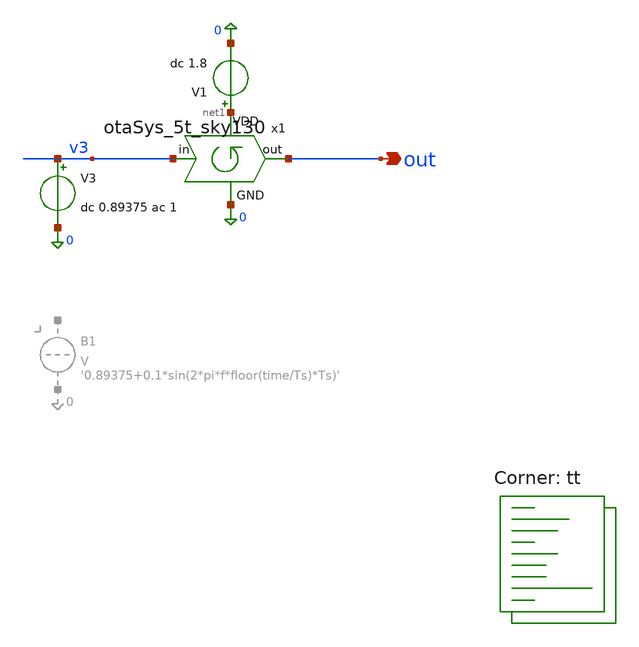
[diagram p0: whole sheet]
** sch_path: xschem/otaSys_5t_sky130_tb.sch
**.subckt otaSys_5t_sky130_tb out
*.opin out
V3 v3 0 dc 0.89375 ac 1
x1 net1 v3 out 0 otaSys_5t_sky130
V1 net1 0 dc 1.8
**** begin user architecture code
.lib $::SKYWATER_MODELS/sky130.lib.spice tt


.control
save all
.param f=5Meg
.param Fs=20Meg
.param Ts={1/Fs}
tran 1n 60000n
write otaSys_5t_sky130_tb_tran.raw
op
print @m.x1.x4.xm2.msky130_fd_pr__nfet_01v8[id] @m.x1.x4.xm4.msky130_fd_pr__pfet_01v8[id]
write otaSys_5t_sky130_tb_op.raw
ac dec 20 1 100meg
write otaSys_5t_sky130_tb_ac.raw
.endc

**** end user architecture code
**.ends

* expanding   symbol:  otaSys_5t_sky130.sym # of pins=4
** sym_path: xschem/otaSys_5t_sky130.sym
** sch_path: xschem/otaSys_5t_sky130.sch
.subckt otaSys_5t_sky130 VDD in out GND
*.opin out
*.ipin in
*.ipin GND
*.ipin VDD
x1 VDD net1 net2 in GND ota_5t_sky130
x2 VDD out net1 net2 GND ota_5t_sky130
x3 VDD net1 net2 out GND ota_5t_sky130
x4 VDD out out net2 GND otaq_5t_sky130
XC1 net1 GND sky130_fd_pr__cap_mim_m3_1 W=30 L=30 MF=4 m=4
XR1 VDD net2 GND sky130_fd_pr__res_high_po_1p41 L=88.83 mult=1 m=1
XR2 net2 GND GND sky130_fd_pr__res_high_po_1p41 L=88.83 mult=1 m=1
XC2 out GND sky130_fd_pr__cap_mim_m3_1 W=24 L=24 MF=1 m=1
XC3 out GND sky130_fd_pr__cap_mim_m3_1 W=24 L=24 MF=1 m=1
.ends


* expanding   symbol:  ota_5t_sky130.sym # of pins=5
** sym_path: xschem/ota_5t_sky130.sym
** sch_path: xschem/ota_5t_sky130.sch
.subckt ota_5t_sky130 VDD VOUT VINP VINN GND
*.ipin VINP
*.ipin VINN
*.opin VOUT
*.ipin VDD
*.ipin GND
XM5 V5 VDD GND GND sky130_fd_pr__nfet_01v8 L=1.475 W=4 nf=1 ad='int((1 + 1)/2) * 4 / 1 * 0.29' as='int((1 + 2)/2) * 4 / 1 * 0.29'
+ pd='2*int((1 + 1)/2) * (4 / 1 + 0.29)' ps='2*int((1 + 2)/2) * (4 / 1 + 0.29)' nrd='0.29 / 4 ' nrs='0.29 / 4 '
+ sa=0 sb=0 sd=0 mult=1 m=1
XM1 net1 VINP V5 GND sky130_fd_pr__nfet_01v8 L=0.5 W=2 nf=1 ad='int((1 + 1)/2) * 2 / 1 * 0.29' as='int((1 + 2)/2) * 2 / 1 * 0.29'
+ pd='2*int((1 + 1)/2) * (2 / 1 + 0.29)' ps='2*int((1 + 2)/2) * (2 / 1 + 0.29)' nrd='0.29 / 2 ' nrs='0.29 / 2 '
+ sa=0 sb=0 sd=0 mult=1 m=1
XM2 VOUT VINN V5 GND sky130_fd_pr__nfet_01v8 L=0.5 W=2 nf=1 ad='int((1 + 1)/2) * 2 / 1 * 0.29' as='int((1 + 2)/2) * 2 / 1 * 0.29'
+ pd='2*int((1 + 1)/2) * (2 / 1 + 0.29)' ps='2*int((1 + 2)/2) * (2 / 1 + 0.29)' nrd='0.29 / 2 ' nrs='0.29 / 2 '
+ sa=0 sb=0 sd=0 mult=1 m=1
XM3 net1 net1 VDD VDD sky130_fd_pr__pfet_01v8 L=0.5 W=5 nf=1 ad='int((1 + 1)/2) * 5 / 1 * 0.29' as='int((1 + 2)/2) * 5 / 1 * 0.29'
+ pd='2*int((1 + 1)/2) * (5 / 1 + 0.29)' ps='2*int((1 + 2)/2) * (5 / 1 + 0.29)' nrd='0.29 / 5 ' nrs='0.29 / 5 '
+ sa=0 sb=0 sd=0 mult=1 m=1
XM4 VOUT net1 VDD VDD sky130_fd_pr__pfet_01v8 L=0.5 W=5 nf=1 ad='int((1 + 1)/2) * 5 / 1 * 0.29' as='int((1 + 2)/2) * 5 / 1 * 0.29'
+ pd='2*int((1 + 1)/2) * (5 / 1 + 0.29)' ps='2*int((1 + 2)/2) * (5 / 1 + 0.29)' nrd='0.29 / 5 ' nrs='0.29 / 5 '
+ sa=0 sb=0 sd=0 mult=1 m=1
XM6 VDD VDD GND GND sky130_fd_pr__nfet_01v8 L=0.5 W=4 nf=1 ad='int((1 + 1)/2) * 4 / 1 * 0.29' as='int((1 + 2)/2) * 4 / 1 * 0.29'
+ pd='2*int((1 + 1)/2) * (4 / 1 + 0.29)' ps='2*int((1 + 2)/2) * (4 / 1 + 0.29)' nrd='0.29 / 4 ' nrs='0.29 / 4 '
+ sa=0 sb=0 sd=0 mult=1 m=1
.ends


* expanding   symbol:  otaq_5t_sky130.sym # of pins=5
** sym_path: xschem/otaq_5t_sky130.sym
** sch_path: xschem/otaq_5t_sky130.sch
.subckt otaq_5t_sky130 VDD VOUT VINP VINN GND
*.ipin VINP
*.ipin VINN
*.opin VOUT
*.ipin VDD
*.ipin GND
XM5 net2 VDD GND GND sky130_fd_pr__nfet_01v8 L=20 W=0.5 nf=1 ad='int((1 + 1)/2) * 0.5 / 1 * 0.29' as='int((1 + 2)/2) * 0.5 / 1 * 0.29'
+ pd='2*int((1 + 1)/2) * (0.5 / 1 + 0.29)' ps='2*int((1 + 2)/2) * (0.5 / 1 + 0.29)' nrd='0.29 / 0.5 ' nrs='0.29 / 0.5 '
+ sa=0 sb=0 sd=0 mult=1 m=1
XM1 net1 VINP net2 GND sky130_fd_pr__nfet_01v8 L=7 W=0.5 nf=1 ad='int((1 + 1)/2) * 0.5 / 1 * 0.29' as='int((1 + 2)/2) * 0.5 / 1 * 0.29'
+ pd='2*int((1 + 1)/2) * (0.5 / 1 + 0.29)' ps='2*int((1 + 2)/2) * (0.5 / 1 + 0.29)' nrd='0.29 / 0.5 ' nrs='0.29 / 0.5 '
+ sa=0 sb=0 sd=0 mult=1 m=1
XM2 VOUT VINN net2 GND sky130_fd_pr__nfet_01v8 L=7 W=0.5 nf=1 ad='int((1 + 1)/2) * 0.5 / 1 * 0.29' as='int((1 + 2)/2) * 0.5 / 1 * 0.29'
+ pd='2*int((1 + 1)/2) * (0.5 / 1 + 0.29)' ps='2*int((1 + 2)/2) * (0.5 / 1 + 0.29)' nrd='0.29 / 0.5 ' nrs='0.29 / 0.5 '
+ sa=0 sb=0 sd=0 mult=1 m=1
XM3 net1 net1 VDD VDD sky130_fd_pr__pfet_01v8 L=7 W=1 nf=1 ad='int((1 + 1)/2) * 1 / 1 * 0.29' as='int((1 + 2)/2) * 1 / 1 * 0.29'
+ pd='2*int((1 + 1)/2) * (1 / 1 + 0.29)' ps='2*int((1 + 2)/2) * (1 / 1 + 0.29)' nrd='0.29 / 1 ' nrs='0.29 / 1 '
+ sa=0 sb=0 sd=0 mult=1 m=1
XM4 VOUT net1 VDD VDD sky130_fd_pr__pfet_01v8 L=7 W=1 nf=1 ad='int((1 + 1)/2) * 1 / 1 * 0.29' as='int((1 + 2)/2) * 1 / 1 * 0.29'
+ pd='2*int((1 + 1)/2) * (1 / 1 + 0.29)' ps='2*int((1 + 2)/2) * (1 / 1 + 0.29)' nrd='0.29 / 1 ' nrs='0.29 / 1 '
+ sa=0 sb=0 sd=0 mult=1 m=1
XM6 VDD VDD GND GND sky130_fd_pr__nfet_01v8 L=0.5 W=1 nf=1 ad='int((1 + 1)/2) * 1 / 1 * 0.29' as='int((1 + 2)/2) * 1 / 1 * 0.29'
+ pd='2*int((1 + 1)/2) * (1 / 1 + 0.29)' ps='2*int((1 + 2)/2) * (1 / 1 + 0.29)' nrd='0.29 / 1 ' nrs='0.29 / 1 '
+ sa=0 sb=0 sd=0 mult=1 m=1
.ends

.end
